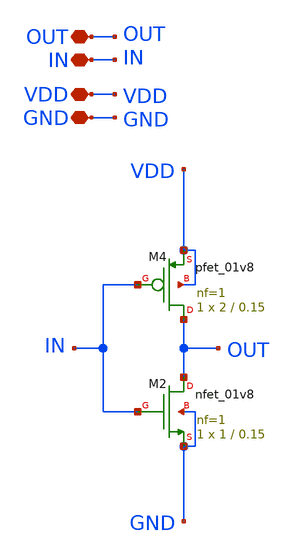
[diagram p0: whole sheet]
** sch_path: xschem/inv.sch
**.subckt inv VDD GND IN OUT
*.iopin VDD
*.iopin GND
*.iopin IN
*.iopin OUT
XM2 OUT IN GND GND sky130_fd_pr__nfet_01v8 L=0.15 W=1 nf=1 ad='int((nf+1)/2) * W/nf * 0.29' as='int((nf+2)/2) * W/nf * 0.29'
+ pd='2*int((nf+1)/2) * (W/nf + 0.29)' ps='2*int((nf+2)/2) * (W/nf + 0.29)' nrd='0.29 / W' nrs='0.29 / W'
+ sa=0 sb=0 sd=0 mult=1 m=1
XM4 OUT IN VDD VDD sky130_fd_pr__pfet_01v8 L=0.15 W=2 nf=1 ad='int((nf+1)/2) * W/nf * 0.29' as='int((nf+2)/2) * W/nf * 0.29'
+ pd='2*int((nf+1)/2) * (W/nf + 0.29)' ps='2*int((nf+2)/2) * (W/nf + 0.29)' nrd='0.29 / W' nrs='0.29 / W'
+ sa=0 sb=0 sd=0 mult=1 m=1
**.ends
.end
